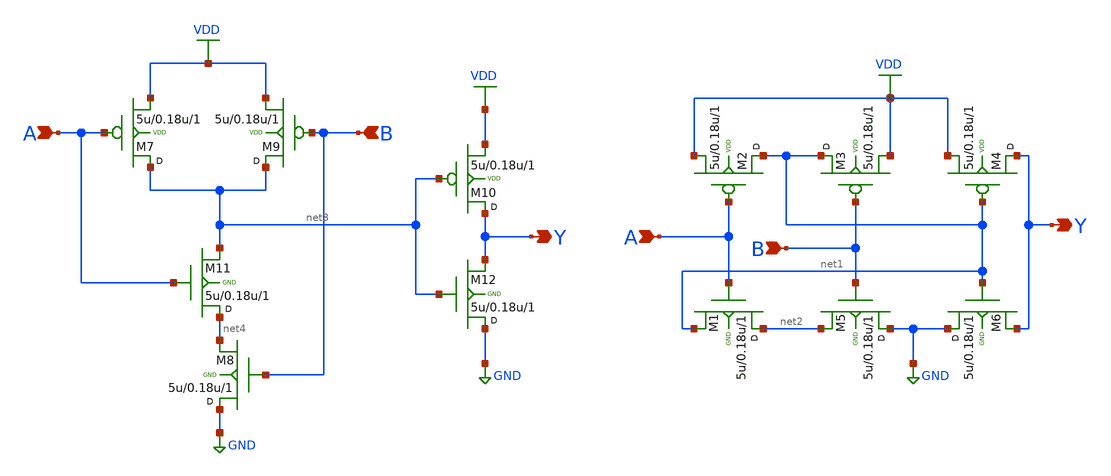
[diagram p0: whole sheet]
** sch_path: sch/AND2.sch
**.subckt AND2 A B Y A B Y
*.ipin A
*.ipin B
*.opin Y
*.ipin A
*.ipin B
*.opin Y
M1 net2 A net1 GND nfet w=5u l=0.18u m=1
M2 net1 A VDD VDD pfet w=5u l=0.18u m=1
M3 net1 B VDD VDD pfet w=5u l=0.18u m=1
M4 Y net1 VDD VDD pfet w=5u l=0.18u m=1
M5 GND B net2 GND nfet w=5u l=0.18u m=1
M6 GND net1 Y GND nfet w=5u l=0.18u m=1
M7 net3 A VDD VDD pfet w=5u l=0.18u m=1
M8 GND B net4 GND nfet w=5u l=0.18u m=1
M9 net3 B VDD VDD pfet w=5u l=0.18u m=1
M10 Y net3 VDD VDD pfet w=5u l=0.18u m=1
M11 net4 A net3 GND nfet w=5u l=0.18u m=1
M12 GND net3 Y GND nfet w=5u l=0.18u m=1
**.ends
.GLOBAL GND
.GLOBAL VDD
.end
